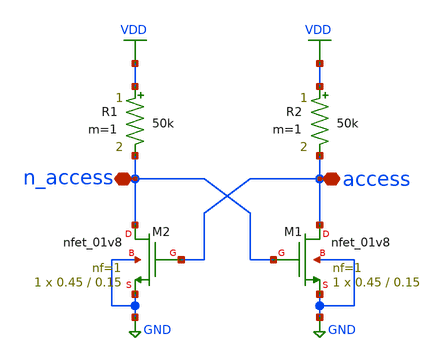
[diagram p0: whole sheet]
** sch_path: analog/schematics/2T2R.sch
**.subckt 2T2R access n_access
*.iopin access
*.iopin n_access
XM1 access n_access GND GND sky130_fd_pr__nfet_01v8 L=0.15 W=0.45 nf=1 ad='int((nf+1)/2) * W/nf * 0.29'
+ as='int((nf+2)/2) * W/nf * 0.29' pd='2*int((nf+1)/2) * (W/nf + 0.29)' ps='2*int((nf+2)/2) * (W/nf + 0.29)'
+ nrd='0.29 / W' nrs='0.29 / W' sa=0 sb=0 sd=0 mult=1 m=1
XM2 n_access access GND GND sky130_fd_pr__nfet_01v8 L=0.15 W=0.45 nf=1 ad='int((nf+1)/2) * W/nf * 0.29'
+ as='int((nf+2)/2) * W/nf * 0.29' pd='2*int((nf+1)/2) * (W/nf + 0.29)' ps='2*int((nf+2)/2) * (W/nf + 0.29)'
+ nrd='0.29 / W' nrs='0.29 / W' sa=0 sb=0 sd=0 mult=1 m=1
R1 VDD n_access 50k m=1
R2 VDD access 50k m=1
**.ends
.GLOBAL VDD
.GLOBAL GND
.end
